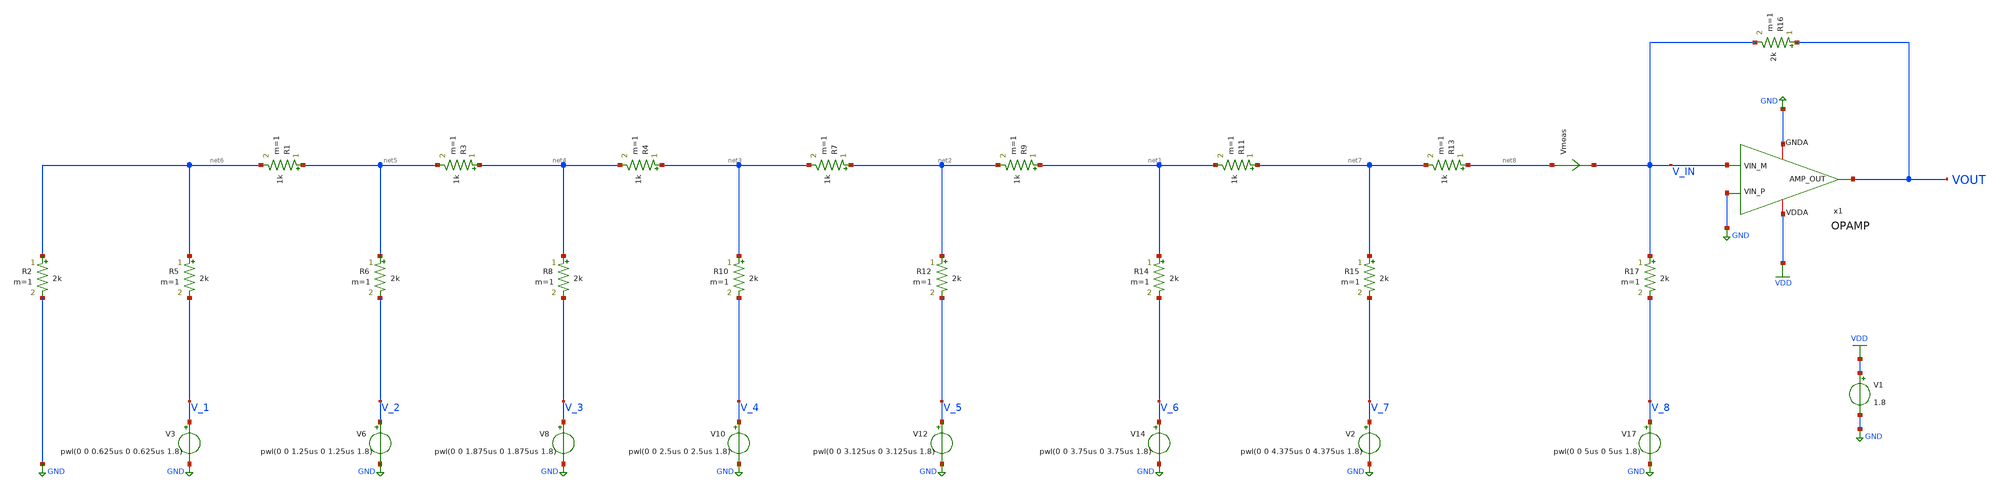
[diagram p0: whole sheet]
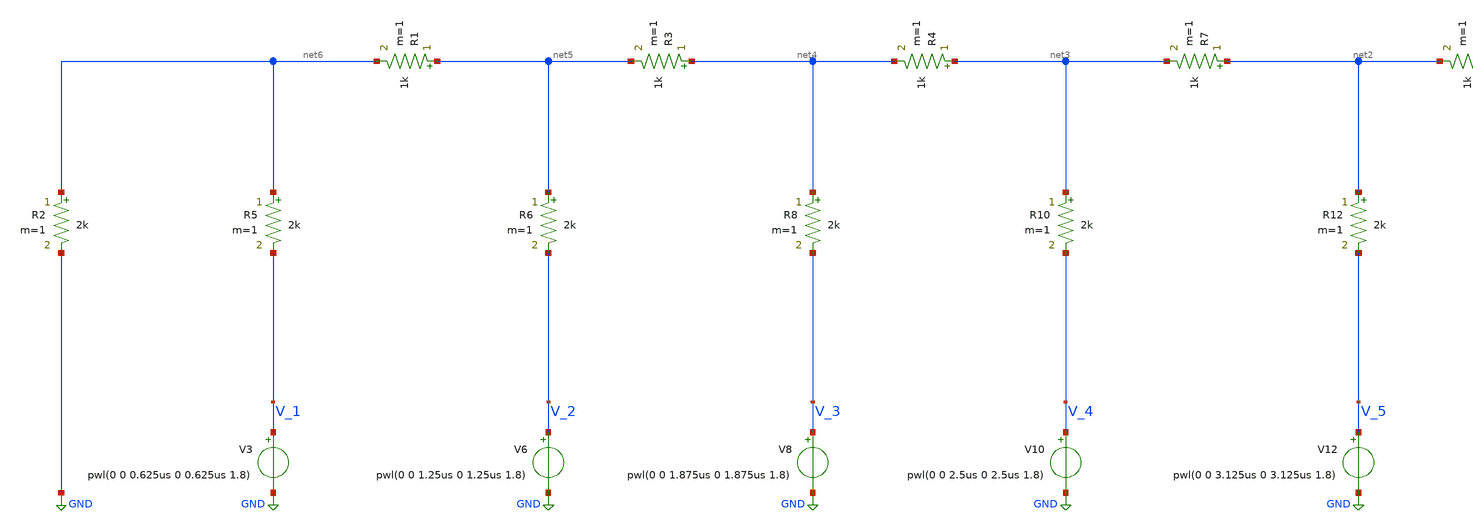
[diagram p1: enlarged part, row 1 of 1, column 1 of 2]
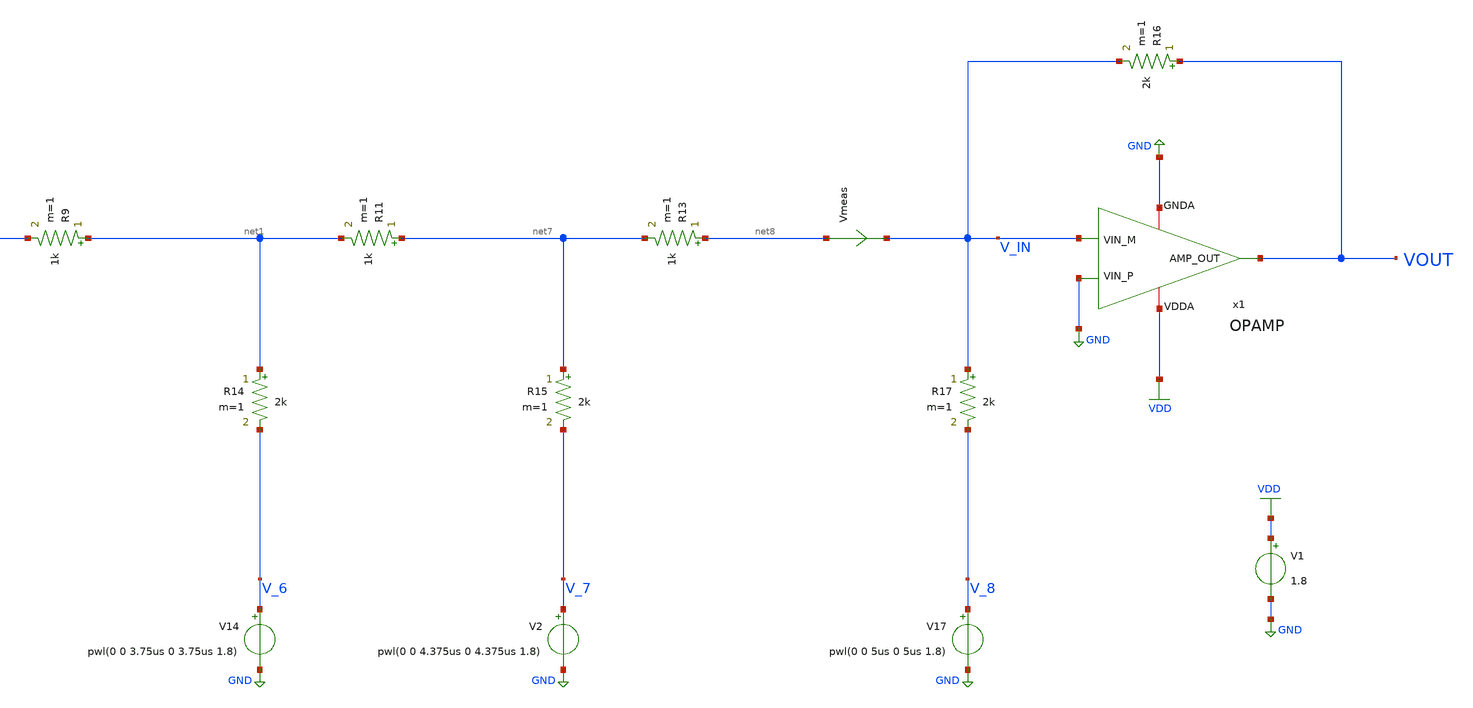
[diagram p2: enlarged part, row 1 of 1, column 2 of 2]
** sch_path: projects/ASU/EEE572/schematic/tb_PWM_gen_3.sch
**.subckt tb_PWM_gen_3
V1 VDD GND 1.8
V3 V_1 GND pwl(0 0 0.625us 0 0.625us 1.8)
x1 VDD VOUT GND V_IN GND OPAMP
V6 V_2 GND pwl(0 0 1.25us 0 1.25us 1.8)
V8 V_3 GND pwl(0 0 1.875us 0 1.875us 1.8)
V10 V_4 GND pwl(0 0 2.5us 0 2.5us 1.8)
V12 V_5 GND pwl(0 0 3.125us 0 3.125us 1.8)
V14 V_6 GND pwl(0 0 3.75us 0 3.75us 1.8)
V2 V_7 GND pwl(0 0 4.375us 0 4.375us 1.8)
V17 V_8 GND pwl(0 0 5us 0 5us 1.8)
Vmeas net8 V_IN 0
.save i(vmeas)
R2 net6 GND 2k m=1
R5 net6 V_1 2k m=1
R6 net5 V_2 2k m=1
R8 net4 V_3 2k m=1
R10 net3 V_4 2k m=1
R12 net2 V_5 2k m=1
R14 net1 V_6 2k m=1
R15 net7 V_7 2k m=1
R16 VOUT V_IN 2k m=1
R17 V_IN V_8 2k m=1
R1 net5 net6 1k m=1
R3 net4 net5 1k m=1
R4 net3 net4 1k m=1
R7 net2 net3 1k m=1
R9 net1 net2 1k m=1
R11 net7 net1 1k m=1
R13 net8 net7 1k m=1
**** begin user architecture code
.lib $::SKYWATER_MODELS/sky130.lib.spice tt



.options method=gear
.options wnflag=1
.options savecurrents

* .include /foss/pdks/sky130A/libs.ref/sky130_fd_sc_hd/spice/sky130_fd_sc_hd.spice

.save v(vout) v(v_1) v(v_2) v(v_3) v(v_4) v(v_5) v(v_6) v(v_7) v(v_in)


.control
  * save all
  * dc V1 0.0 2.0 0.005
  tran 0.10ns 5.2us
  remzerovec
  write tb_PWM_gen_3.raw
  set appendwrite

.endc





**** end user architecture code
**.ends

* expanding   symbol:  OPAMP.sym # of pins=5
** sym_path: projects/ASU/EEE572/schematic/OPAMP.sym
** sch_path: projects/ASU/EEE572/schematic/OPAMP.sch
.subckt OPAMP VDDA AMP_OUT VIN_P VIN_M GNDA
*.iopin GNDA
*.iopin VDDA
*.iopin VIN_M
*.iopin VIN_P
*.iopin AMP_OUT
XM1 V_REF V_REF V_RES GNDA sky130_fd_pr__nfet_01v8 L=0.3 W=16 nf=8 ad='int((nf+1)/2) * W/nf * 0.29' as='int((nf+2)/2) * W/nf * 0.29'
+ pd='2*int((nf+1)/2) * (W/nf + 0.29)' ps='2*int((nf+2)/2) * (W/nf + 0.29)' nrd='0.29 / W' nrs='0.29 / W'
+ sa=0 sb=0 sd=0 mult=1 m=1
XM2 V_REF_MIR V_REF_MIR GNDA GNDA sky130_fd_pr__nfet_01v8 L=0.3 W=4 nf=2 ad='int((nf+1)/2) * W/nf * 0.29'
+ as='int((nf+2)/2) * W/nf * 0.29' pd='2*int((nf+1)/2) * (W/nf + 0.29)' ps='2*int((nf+2)/2) * (W/nf + 0.29)'
+ nrd='0.29 / W' nrs='0.29 / W' sa=0 sb=0 sd=0 mult=1 m=1
XM5 START_UP V_REF_MIR GNDA GNDA sky130_fd_pr__nfet_01v8 L=0.3 W=4 nf=2 ad='int((nf+1)/2) * W/nf * 0.29'
+ as='int((nf+2)/2) * W/nf * 0.29' pd='2*int((nf+1)/2) * (W/nf + 0.29)' ps='2*int((nf+2)/2) * (W/nf + 0.29)'
+ nrd='0.29 / W' nrs='0.29 / W' sa=0 sb=0 sd=0 mult=1 m=1
XM7 Vbiasp START_UP V_REF_MIR GNDA sky130_fd_pr__nfet_01v8 L=0.3 W=4 nf=2 ad='int((nf+1)/2) * W/nf * 0.29'
+ as='int((nf+2)/2) * W/nf * 0.29' pd='2*int((nf+1)/2) * (W/nf + 0.29)' ps='2*int((nf+2)/2) * (W/nf + 0.29)'
+ nrd='0.29 / W' nrs='0.29 / W' sa=0 sb=0 sd=0 mult=1 m=1
XM6 START_UP START_UP VDD VDD sky130_fd_pr__pfet_01v8 L=20 W=0.5 nf=1 ad='int((nf+1)/2) * W/nf * 0.29'
+ as='int((nf+2)/2) * W/nf * 0.29' pd='2*int((nf+1)/2) * (W/nf + 0.29)' ps='2*int((nf+2)/2) * (W/nf + 0.29)'
+ nrd='0.29 / W' nrs='0.29 / W' sa=0 sb=0 sd=0 mult=1 m=1
XM3 V_REF Vbiasp VDDA VDDA sky130_fd_pr__pfet_01v8 L=0.3 W=12 nf=6 ad='int((nf+1)/2) * W/nf * 0.29' as='int((nf+2)/2) * W/nf * 0.29'
+ pd='2*int((nf+1)/2) * (W/nf + 0.29)' ps='2*int((nf+2)/2) * (W/nf + 0.29)' nrd='0.29 / W' nrs='0.29 / W'
+ sa=0 sb=0 sd=0 mult=1 m=1
XM4 V_REF_MIR Vbiasp VDDA VDDA sky130_fd_pr__pfet_01v8 L=0.3 W=12 nf=6 ad='int((nf+1)/2) * W/nf * 0.29'
+ as='int((nf+2)/2) * W/nf * 0.29' pd='2*int((nf+1)/2) * (W/nf + 0.29)' ps='2*int((nf+2)/2) * (W/nf + 0.29)'
+ nrd='0.29 / W' nrs='0.29 / W' sa=0 sb=0 sd=0 mult=1 m=1
XM8 Vbiasp V_REF_MIR GNDA GNDA sky130_fd_pr__nfet_01v8 L=0.3 W=4 nf=2 ad='int((nf+1)/2) * W/nf * 0.29'
+ as='int((nf+2)/2) * W/nf * 0.29' pd='2*int((nf+1)/2) * (W/nf + 0.29)' ps='2*int((nf+2)/2) * (W/nf + 0.29)'
+ nrd='0.29 / W' nrs='0.29 / W' sa=0 sb=0 sd=0 mult=1 m=1
XM9 Vbiasp_MIR V_REF GNDA GNDA sky130_fd_pr__nfet_01v8 L=0.3 W=4 nf=2 ad='int((nf+1)/2) * W/nf * 0.29'
+ as='int((nf+2)/2) * W/nf * 0.29' pd='2*int((nf+1)/2) * (W/nf + 0.29)' ps='2*int((nf+2)/2) * (W/nf + 0.29)'
+ nrd='0.29 / W' nrs='0.29 / W' sa=0 sb=0 sd=0 mult=1 m=1
XM10 Vbiasp Vbiasp_MIR VDDA VDDA sky130_fd_pr__pfet_01v8 L=0.3 W=12 nf=6 ad='int((nf+1)/2) * W/nf * 0.29'
+ as='int((nf+2)/2) * W/nf * 0.29' pd='2*int((nf+1)/2) * (W/nf + 0.29)' ps='2*int((nf+2)/2) * (W/nf + 0.29)'
+ nrd='0.29 / W' nrs='0.29 / W' sa=0 sb=0 sd=0 mult=1 m=1
XM11 Vbiasp_MIR Vbiasp_MIR VDDA VDDA sky130_fd_pr__pfet_01v8 L=0.3 W=12 nf=6 ad='int((nf+1)/2) * W/nf * 0.29'
+ as='int((nf+2)/2) * W/nf * 0.29' pd='2*int((nf+1)/2) * (W/nf + 0.29)' ps='2*int((nf+2)/2) * (W/nf + 0.29)'
+ nrd='0.29 / W' nrs='0.29 / W' sa=0 sb=0 sd=0 mult=1 m=1
XM12 Vbias3 Vbias3 GNDA GNDA sky130_fd_pr__nfet_01v8 L=4 W=4 nf=1 ad='int((nf+1)/2) * W/nf * 0.29' as='int((nf+2)/2) * W/nf * 0.29'
+ pd='2*int((nf+1)/2) * (W/nf + 0.29)' ps='2*int((nf+2)/2) * (W/nf + 0.29)' nrd='0.29 / W' nrs='0.29 / W'
+ sa=0 sb=0 sd=0 mult=1 m=1
XM13 Vbias3 Vbiasp VDDA VDDA sky130_fd_pr__pfet_01v8 L=0.3 W=12 nf=6 ad='int((nf+1)/2) * W/nf * 0.29'
+ as='int((nf+2)/2) * W/nf * 0.29' pd='2*int((nf+1)/2) * (W/nf + 0.29)' ps='2*int((nf+2)/2) * (W/nf + 0.29)'
+ nrd='0.29 / W' nrs='0.29 / W' sa=0 sb=0 sd=0 mult=1 m=1
XM14 net1 Vbias1 VDDA VDDA sky130_fd_pr__pfet_01v8 L=0.3 W=12 nf=6 ad='int((nf+1)/2) * W/nf * 0.29' as='int((nf+2)/2) * W/nf * 0.29'
+ pd='2*int((nf+1)/2) * (W/nf + 0.29)' ps='2*int((nf+2)/2) * (W/nf + 0.29)' nrd='0.29 / W' nrs='0.29 / W'
+ sa=0 sb=0 sd=0 mult=1 m=1
XM15 Vhigh Vbias1 VDDA VDDA sky130_fd_pr__pfet_01v8 L=0.3 W=12 nf=6 ad='int((nf+1)/2) * W/nf * 0.29'
+ as='int((nf+2)/2) * W/nf * 0.29' pd='2*int((nf+1)/2) * (W/nf + 0.29)' ps='2*int((nf+2)/2) * (W/nf + 0.29)'
+ nrd='0.29 / W' nrs='0.29 / W' sa=0 sb=0 sd=0 mult=1 m=1
XM16 Vncas Vbias2 net1 VDDA sky130_fd_pr__pfet_01v8 L=0.3 W=12 nf=6 ad='int((nf+1)/2) * W/nf * 0.29'
+ as='int((nf+2)/2) * W/nf * 0.29' pd='2*int((nf+1)/2) * (W/nf + 0.29)' ps='2*int((nf+2)/2) * (W/nf + 0.29)'
+ nrd='0.29 / W' nrs='0.29 / W' sa=0 sb=0 sd=0 mult=1 m=1
XM17 Vbias1 Vbias2 Vhigh VDDA sky130_fd_pr__pfet_01v8 L=0.3 W=12 nf=6 ad='int((nf+1)/2) * W/nf * 0.29'
+ as='int((nf+2)/2) * W/nf * 0.29' pd='2*int((nf+1)/2) * (W/nf + 0.29)' ps='2*int((nf+2)/2) * (W/nf + 0.29)'
+ nrd='0.29 / W' nrs='0.29 / W' sa=0 sb=0 sd=0 mult=1 m=1
XM18 net2 Vbias4 GNDA GNDA sky130_fd_pr__nfet_01v8 L=0.3 W=4 nf=2 ad='int((nf+1)/2) * W/nf * 0.29' as='int((nf+2)/2) * W/nf * 0.29'
+ pd='2*int((nf+1)/2) * (W/nf + 0.29)' ps='2*int((nf+2)/2) * (W/nf + 0.29)' nrd='0.29 / W' nrs='0.29 / W'
+ sa=0 sb=0 sd=0 mult=1 m=1
XM19 Vncas Vncas Vncas_btw GNDA sky130_fd_pr__nfet_01v8 L=0.3 W=4 nf=2 ad='int((nf+1)/2) * W/nf * 0.29'
+ as='int((nf+2)/2) * W/nf * 0.29' pd='2*int((nf+1)/2) * (W/nf + 0.29)' ps='2*int((nf+2)/2) * (W/nf + 0.29)'
+ nrd='0.29 / W' nrs='0.29 / W' sa=0 sb=0 sd=0 mult=1 m=1
XM20 Vncas_btw Vbias3 net3 GNDA sky130_fd_pr__nfet_01v8 L=0.3 W=4 nf=2 ad='int((nf+1)/2) * W/nf * 0.29'
+ as='int((nf+2)/2) * W/nf * 0.29' pd='2*int((nf+1)/2) * (W/nf + 0.29)' ps='2*int((nf+2)/2) * (W/nf + 0.29)'
+ nrd='0.29 / W' nrs='0.29 / W' sa=0 sb=0 sd=0 mult=1 m=1
XM21 net3 Vncas_btw GNDA GNDA sky130_fd_pr__nfet_01v8 L=0.3 W=4 nf=2 ad='int((nf+1)/2) * W/nf * 0.29'
+ as='int((nf+2)/2) * W/nf * 0.29' pd='2*int((nf+1)/2) * (W/nf + 0.29)' ps='2*int((nf+2)/2) * (W/nf + 0.29)'
+ nrd='0.29 / W' nrs='0.29 / W' sa=0 sb=0 sd=0 mult=1 m=1
XM25 Vbias4 Vbiasp VDDA VDDA sky130_fd_pr__pfet_01v8 L=0.3 W=12 nf=6 ad='int((nf+1)/2) * W/nf * 0.29'
+ as='int((nf+2)/2) * W/nf * 0.29' pd='2*int((nf+1)/2) * (W/nf + 0.29)' ps='2*int((nf+2)/2) * (W/nf + 0.29)'
+ nrd='0.29 / W' nrs='0.29 / W' sa=0 sb=0 sd=0 mult=1 m=1
XM27 Vbias4 Vbias3 Vlow GNDA sky130_fd_pr__nfet_01v8 L=0.3 W=4 nf=2 ad='int((nf+1)/2) * W/nf * 0.29'
+ as='int((nf+2)/2) * W/nf * 0.29' pd='2*int((nf+1)/2) * (W/nf + 0.29)' ps='2*int((nf+2)/2) * (W/nf + 0.29)'
+ nrd='0.29 / W' nrs='0.29 / W' sa=0 sb=0 sd=0 mult=1 m=1
XM28 Vlow Vbias4 GNDA GNDA sky130_fd_pr__nfet_01v8 L=0.3 W=4 nf=2 ad='int((nf+1)/2) * W/nf * 0.29' as='int((nf+2)/2) * W/nf * 0.29'
+ pd='2*int((nf+1)/2) * (W/nf + 0.29)' ps='2*int((nf+2)/2) * (W/nf + 0.29)' nrd='0.29 / W' nrs='0.29 / W'
+ sa=0 sb=0 sd=0 mult=1 m=1
XM29 Vds2 Vgs2 VDDA VDDA sky130_fd_pr__pfet_01v8 L=0.15 W=12 nf=6 ad='int((nf+1)/2) * W/nf * 0.29' as='int((nf+2)/2) * W/nf * 0.29'
+ pd='2*int((nf+1)/2) * (W/nf + 0.29)' ps='2*int((nf+2)/2) * (W/nf + 0.29)' nrd='0.29 / W' nrs='0.29 / W'
+ sa=0 sb=0 sd=0 mult=1 m=1
XM30 Vgs2 Vbias2 Vds2 VDDA sky130_fd_pr__pfet_01v8 L=0.15 W=12 nf=6 ad='int((nf+1)/2) * W/nf * 0.29'
+ as='int((nf+2)/2) * W/nf * 0.29' pd='2*int((nf+1)/2) * (W/nf + 0.29)' ps='2*int((nf+2)/2) * (W/nf + 0.29)'
+ nrd='0.29 / W' nrs='0.29 / W' sa=0 sb=0 sd=0 mult=1 m=1
XM31 Vpcas Vbias3 Vds3 GNDA sky130_fd_pr__nfet_01v8 L=0.3 W=4 nf=2 ad='int((nf+1)/2) * W/nf * 0.29' as='int((nf+2)/2) * W/nf * 0.29'
+ pd='2*int((nf+1)/2) * (W/nf + 0.29)' ps='2*int((nf+2)/2) * (W/nf + 0.29)' nrd='0.29 / W' nrs='0.29 / W'
+ sa=0 sb=0 sd=0 mult=1 m=1
XM32 Vds3 Vbias4 GNDA GNDA sky130_fd_pr__nfet_01v8 L=0.3 W=4 nf=2 ad='int((nf+1)/2) * W/nf * 0.29' as='int((nf+2)/2) * W/nf * 0.29'
+ pd='2*int((nf+1)/2) * (W/nf + 0.29)' ps='2*int((nf+2)/2) * (W/nf + 0.29)' nrd='0.29 / W' nrs='0.29 / W'
+ sa=0 sb=0 sd=0 mult=1 m=1
XM33 Vpcas Vpcas Vgs2 VDDA sky130_fd_pr__pfet_01v8 L=0.15 W=12 nf=1 ad='int((nf+1)/2) * W/nf * 0.29'
+ as='int((nf+2)/2) * W/nf * 0.29' pd='2*int((nf+1)/2) * (W/nf + 0.29)' ps='2*int((nf+2)/2) * (W/nf + 0.29)'
+ nrd='0.29 / W' nrs='0.29 / W' sa=0 sb=0 sd=0 mult=1 m=1
XM22 Vbias1 Vbias3 net2 GNDA sky130_fd_pr__nfet_01v8 L=0.3 W=4 nf=2 ad='int((nf+1)/2) * W/nf * 0.29'
+ as='int((nf+2)/2) * W/nf * 0.29' pd='2*int((nf+1)/2) * (W/nf + 0.29)' ps='2*int((nf+2)/2) * (W/nf + 0.29)'
+ nrd='0.29 / W' nrs='0.29 / W' sa=0 sb=0 sd=0 mult=1 m=1
XM23 Vbias2 Vbias2 VDDA VDDA sky130_fd_pr__pfet_01v8 L=1.5 W=12 nf=1 ad='int((nf+1)/2) * W/nf * 0.29'
+ as='int((nf+2)/2) * W/nf * 0.29' pd='2*int((nf+1)/2) * (W/nf + 0.29)' ps='2*int((nf+2)/2) * (W/nf + 0.29)'
+ nrd='0.29 / W' nrs='0.29 / W' sa=0 sb=0 sd=0 mult=1 m=1
XM24 net4 Vbias4 GNDA GNDA sky130_fd_pr__nfet_01v8 L=0.3 W=4 nf=2 ad='int((nf+1)/2) * W/nf * 0.29' as='int((nf+2)/2) * W/nf * 0.29'
+ pd='2*int((nf+1)/2) * (W/nf + 0.29)' ps='2*int((nf+2)/2) * (W/nf + 0.29)' nrd='0.29 / W' nrs='0.29 / W'
+ sa=0 sb=0 sd=0 mult=1 m=1
XM26 Vbias2 Vbias3 net4 GNDA sky130_fd_pr__nfet_01v8 L=0.3 W=4 nf=2 ad='int((nf+1)/2) * W/nf * 0.29'
+ as='int((nf+2)/2) * W/nf * 0.29' pd='2*int((nf+1)/2) * (W/nf + 0.29)' ps='2*int((nf+2)/2) * (W/nf + 0.29)'
+ nrd='0.29 / W' nrs='0.29 / W' sa=0 sb=0 sd=0 mult=1 m=1
XC1 Vbiasp VDDA sky130_fd_pr__cap_mim_m3_1 W=2 L=2 MF=4 m=4
XR1 GNDA V_RES GNDA sky130_fd_pr__res_high_po_0p35 L=10 mult=1 m=1
XM34 V_tail_btw Vbias4 GNDA GNDA sky130_fd_pr__nfet_01v8 L=0.3 W=12 nf=4 ad='int((nf+1)/2) * W/nf * 0.29'
+ as='int((nf+2)/2) * W/nf * 0.29' pd='2*int((nf+1)/2) * (W/nf + 0.29)' ps='2*int((nf+2)/2) * (W/nf + 0.29)'
+ nrd='0.29 / W' nrs='0.29 / W' sa=0 sb=0 sd=0 mult=3 m=3
XM35 Vp Vbias3 V_tail_btw GNDA sky130_fd_pr__nfet_01v8 L=0.3 W=12 nf=4 ad='int((nf+1)/2) * W/nf * 0.29'
+ as='int((nf+2)/2) * W/nf * 0.29' pd='2*int((nf+1)/2) * (W/nf + 0.29)' ps='2*int((nf+2)/2) * (W/nf + 0.29)'
+ nrd='0.29 / W' nrs='0.29 / W' sa=0 sb=0 sd=0 mult=3 m=3
XM36 Vd1 VIN_P Vp GNDA sky130_fd_pr__nfet_01v8 L=0.3 W=12 nf=4 ad='int((nf+1)/2) * W/nf * 0.29' as='int((nf+2)/2) * W/nf * 0.29'
+ pd='2*int((nf+1)/2) * (W/nf + 0.29)' ps='2*int((nf+2)/2) * (W/nf + 0.29)' nrd='0.29 / W' nrs='0.29 / W'
+ sa=0 sb=0 sd=0 mult=2 m=2
XM37 Vd2 VIN_M Vp GNDA sky130_fd_pr__nfet_01v8 L=0.3 W=12 nf=4 ad='int((nf+1)/2) * W/nf * 0.29' as='int((nf+2)/2) * W/nf * 0.29'
+ pd='2*int((nf+1)/2) * (W/nf + 0.29)' ps='2*int((nf+2)/2) * (W/nf + 0.29)' nrd='0.29 / W' nrs='0.29 / W'
+ sa=0 sb=0 sd=0 mult=2 m=2
XM38 AMP_MIR Vb1 Vd1 GNDA sky130_fd_pr__nfet_01v8 L=0.3 W=12 nf=4 ad='int((nf+1)/2) * W/nf * 0.29' as='int((nf+2)/2) * W/nf * 0.29'
+ pd='2*int((nf+1)/2) * (W/nf + 0.29)' ps='2*int((nf+2)/2) * (W/nf + 0.29)' nrd='0.29 / W' nrs='0.29 / W'
+ sa=0 sb=0 sd=0 mult=2 m=2
XM39 AMP_OUT Vb1 Vd2 GNDA sky130_fd_pr__nfet_01v8 L=0.3 W=12 nf=4 ad='int((nf+1)/2) * W/nf * 0.29' as='int((nf+2)/2) * W/nf * 0.29'
+ pd='2*int((nf+1)/2) * (W/nf + 0.29)' ps='2*int((nf+2)/2) * (W/nf + 0.29)' nrd='0.29 / W' nrs='0.29 / W'
+ sa=0 sb=0 sd=0 mult=2 m=2
XM40 net6 AMP_MIR VDDA VDDA sky130_fd_pr__pfet_01v8 L=0.3 W=12 nf=4 ad='int((nf+1)/2) * W/nf * 0.29'
+ as='int((nf+2)/2) * W/nf * 0.29' pd='2*int((nf+1)/2) * (W/nf + 0.29)' ps='2*int((nf+2)/2) * (W/nf + 0.29)'
+ nrd='0.29 / W' nrs='0.29 / W' sa=0 sb=0 sd=0 mult=6 m=6
XM41 net5 AMP_MIR VDDA VDDA sky130_fd_pr__pfet_01v8 L=0.3 W=12 nf=4 ad='int((nf+1)/2) * W/nf * 0.29'
+ as='int((nf+2)/2) * W/nf * 0.29' pd='2*int((nf+1)/2) * (W/nf + 0.29)' ps='2*int((nf+2)/2) * (W/nf + 0.29)'
+ nrd='0.29 / W' nrs='0.29 / W' sa=0 sb=0 sd=0 mult=6 m=6
XM42 AMP_OUT Vbias2 net6 VDDA sky130_fd_pr__pfet_01v8 L=0.3 W=12 nf=4 ad='int((nf+1)/2) * W/nf * 0.29'
+ as='int((nf+2)/2) * W/nf * 0.29' pd='2*int((nf+1)/2) * (W/nf + 0.29)' ps='2*int((nf+2)/2) * (W/nf + 0.29)'
+ nrd='0.29 / W' nrs='0.29 / W' sa=0 sb=0 sd=0 mult=6 m=6
XM43 AMP_MIR Vbias2 net5 VDDA sky130_fd_pr__pfet_01v8 L=0.3 W=12 nf=4 ad='int((nf+1)/2) * W/nf * 0.29'
+ as='int((nf+2)/2) * W/nf * 0.29' pd='2*int((nf+1)/2) * (W/nf + 0.29)' ps='2*int((nf+2)/2) * (W/nf + 0.29)'
+ nrd='0.29 / W' nrs='0.29 / W' sa=0 sb=0 sd=0 mult=6 m=6
XM44 Vb1 Vb1 Vp GNDA sky130_fd_pr__nfet_01v8 L=1 W=1 nf=1 ad='int((nf+1)/2) * W/nf * 0.29' as='int((nf+2)/2) * W/nf * 0.29'
+ pd='2*int((nf+1)/2) * (W/nf + 0.29)' ps='2*int((nf+2)/2) * (W/nf + 0.29)' nrd='0.29 / W' nrs='0.29 / W'
+ sa=0 sb=0 sd=0 mult=1 m=1
XM45 net7 Vbias1 VDDA VDDA sky130_fd_pr__pfet_01v8 L=0.3 W=12 nf=4 ad='int((nf+1)/2) * W/nf * 0.29' as='int((nf+2)/2) * W/nf * 0.29'
+ pd='2*int((nf+1)/2) * (W/nf + 0.29)' ps='2*int((nf+2)/2) * (W/nf + 0.29)' nrd='0.29 / W' nrs='0.29 / W'
+ sa=0 sb=0 sd=0 mult=1 m=1
XM46 Vb1 Vbias2 net7 VDDA sky130_fd_pr__pfet_01v8 L=0.3 W=12 nf=4 ad='int((nf+1)/2) * W/nf * 0.29' as='int((nf+2)/2) * W/nf * 0.29'
+ pd='2*int((nf+1)/2) * (W/nf + 0.29)' ps='2*int((nf+2)/2) * (W/nf + 0.29)' nrd='0.29 / W' nrs='0.29 / W'
+ sa=0 sb=0 sd=0 mult=1 m=1
.ends

.GLOBAL GND
.GLOBAL VDD
.end
